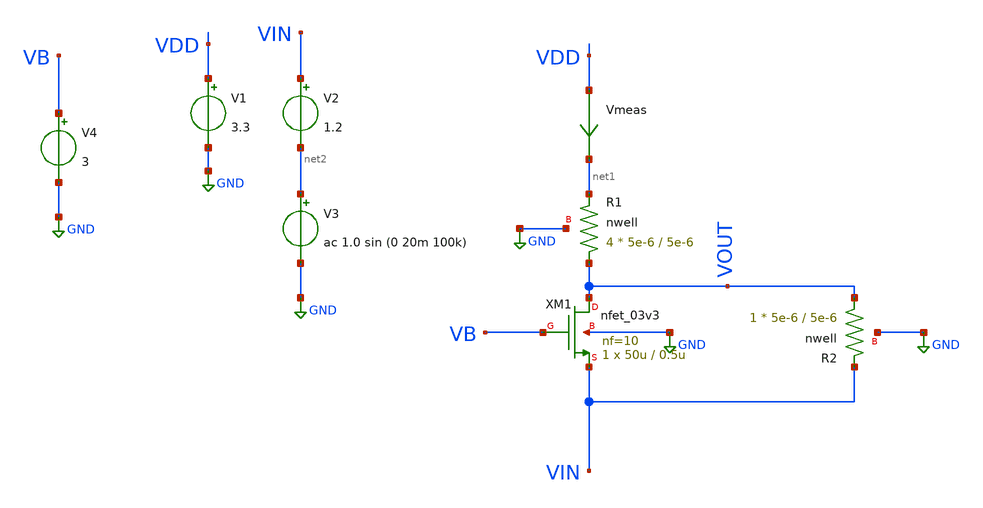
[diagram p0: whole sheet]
** sch_path: simple_amp2.sch
**.subckt simple_amp2
XM1 VOUT VB VIN GND nfet_03v3 L=0.5u W=50u nf=10 ad='int((nf+1)/2) * W/nf * 0.18u' as='int((nf+2)/2) * W/nf * 0.18u'
+ pd='2*int((nf+1)/2) * (W/nf + 0.18u)' ps='2*int((nf+2)/2) * (W/nf + 0.18u)' nrd='0.18u / W' nrs='0.18u / W'
+ sa=0 sb=0 sd=0 m=1
Vmeas VDD net1 0
.save i(vmeas)
V1 VDD GND 3.3
V2 VIN net2 1.2
XR1 VOUT net1 GND nwell r_width=5e-6 r_length=5e-6 m=4
XR2 VOUT VIN GND nwell r_width=5e-6 r_length=5e-6 m=1
V3 net2 GND ac 1.0 sin (0 20m 100k)
V4 VB GND 3
**** begin user architecture code

.include $::180MCU_MODELS/design.ngspice
*.lib $::180MCU_MODELS/sm141064.ngspice statistical
*.lib $::180MCU_MODELS/sm141064.ngspice res_statistical
.lib $::180MCU_MODELS/sm141064.ngspice typical
.lib $::180MCU_MODELS/sm141064.ngspice res_typical
.lib $::180MCU_MODELS/sm141064.ngspice moscap_typical
.lib $::180MCU_MODELS/sm141064.ngspice bjt_typical
.lib $::180MCU_MODELS/sm141064.ngspice diode_typical
.lib $::180MCU_MODELS/sm141064.ngspice mimcap_typical
.TEMP 27

.param   sw_stat_global = 1   sw_stat_mism = 1  mc_skew = 3  res_mc_skew = 3  cap_mc_skew = 3
+  fnoicor = 1



.control
save all
dc V2 0 3.3 0.01


plot v(VOUT) deriv(v(VOUT))
plot v(VOUT) (v(VB)-v(VIN)) deriv(v(VOUT)) (v(VOUT)-v(VIN))
plot i(Vmeas)
plot deriv(v(VOUT))
tran 10ns 20u
plot (v(VOUT)-2.083) (v(VIN)-1.2)
plot fft((v(VOUT))) fft((v(VIN)))
ac dec 20 1 50G
plot v(VOUT)
.endc

**** end user architecture code
**.ends
.GLOBAL GND
.end
